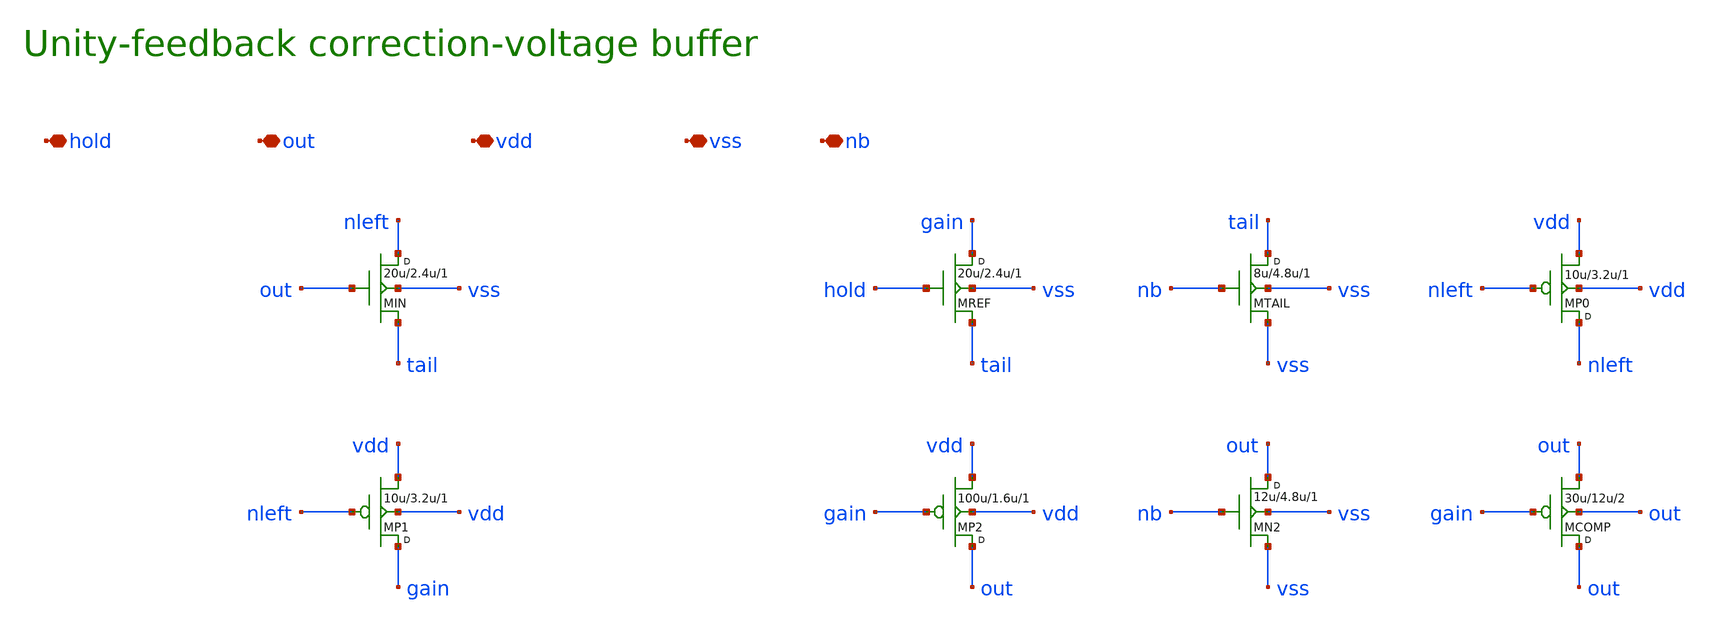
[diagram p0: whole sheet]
** sch_path: ICMC/schematic/icm_buffer08.sch
**.subckt icm_buffer08 hold out vdd vss nb
*.iopin hold
*.iopin out
*.iopin vdd
*.iopin vss
*.iopin nb
MIN nleft out tail vss N w=20u l=2.4u m=1
MREF gain hold tail vss N w=20u l=2.4u m=1
MTAIL tail nb vss vss N w=8u l=4.8u m=1
MP0 nleft nleft vdd vdd P w=10u l=3.2u m=1
MP1 gain nleft vdd vdd P w=10u l=3.2u m=1
MP2 out gain vdd vdd P w=100u l=1.6u m=1
MN2 out nb vss vss N w=12u l=4.8u m=1
MCOMP out gain out out P w=30u l=12u m=2
**.ends
.end
